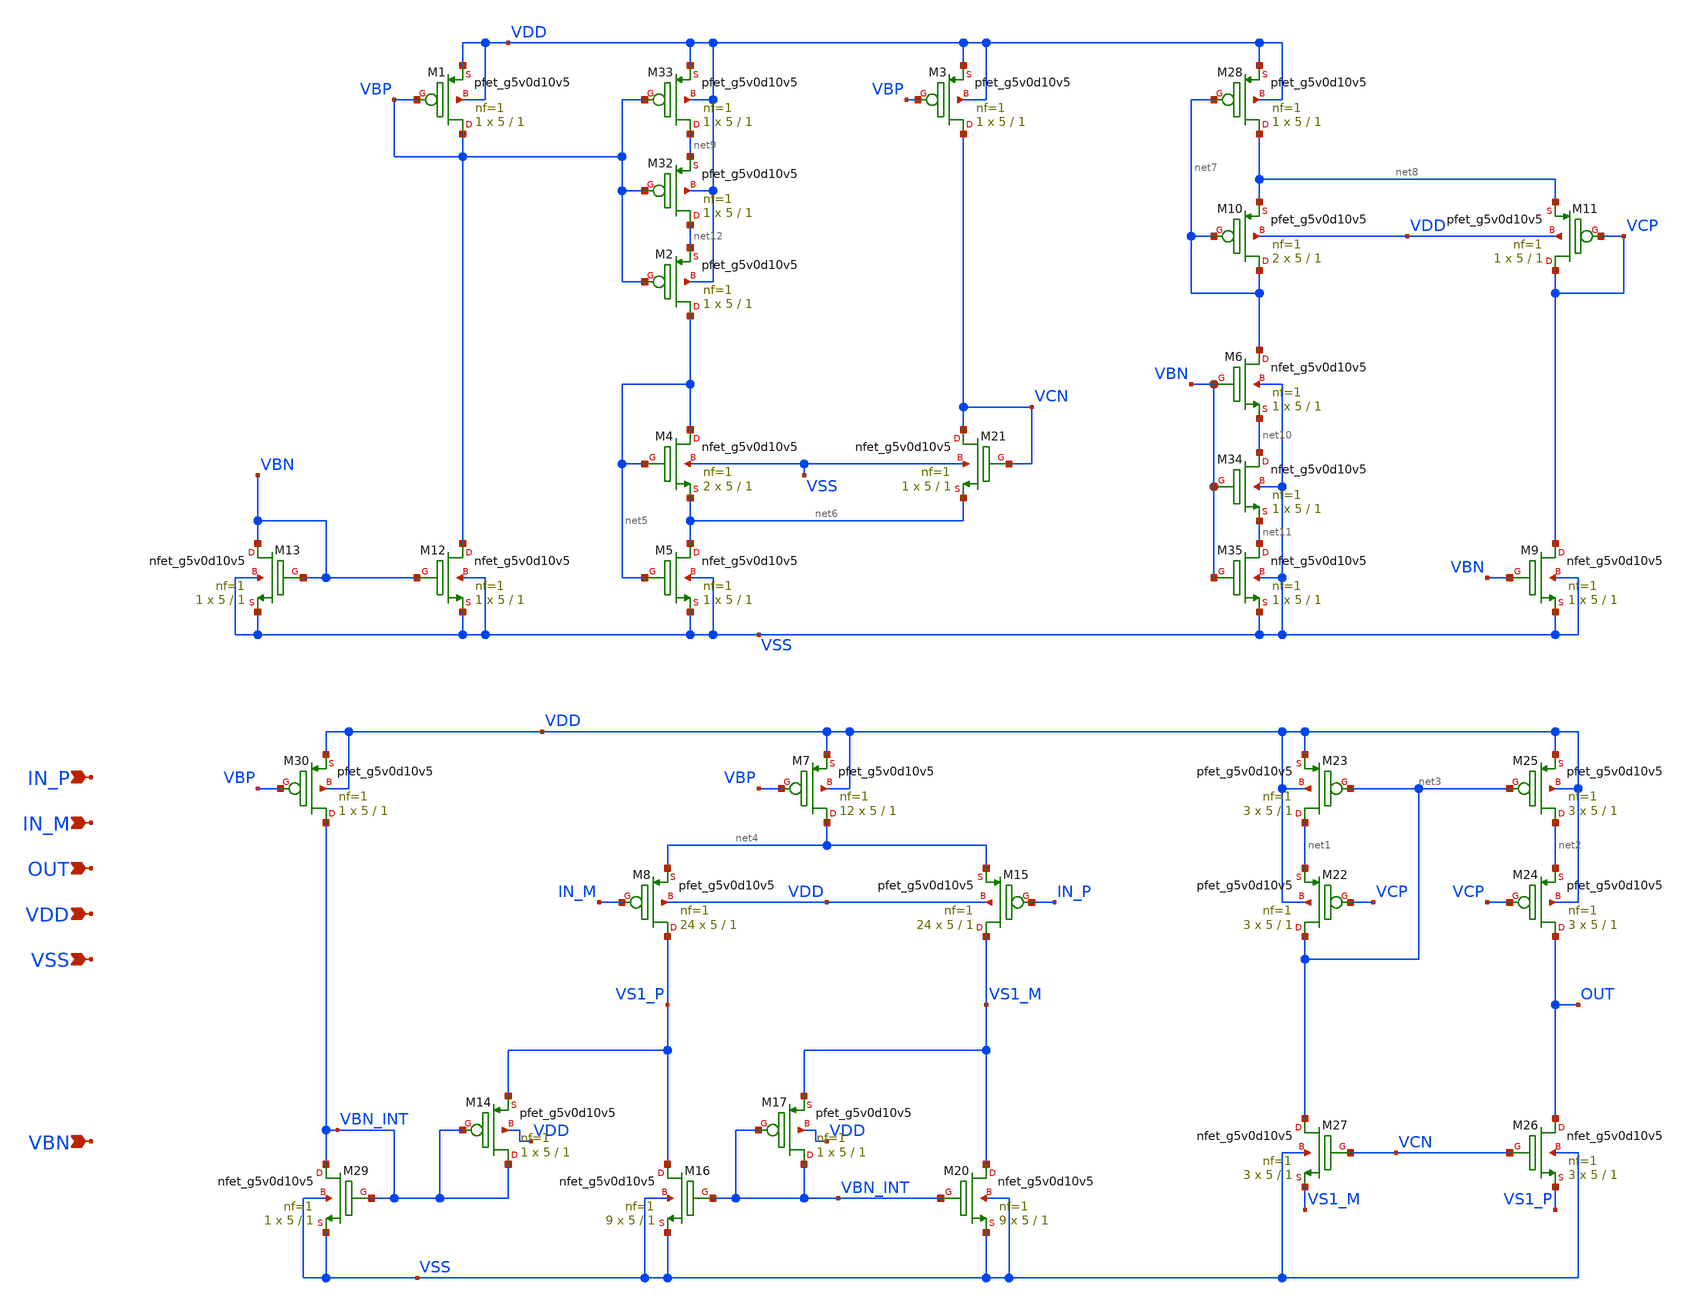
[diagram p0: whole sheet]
** sch_path: design/folded-cascode-p-in/folded_cascode_p_in.sch
**.subckt folded_cascode_p_in IN_P IN_M OUT VDD VSS VBN
*.ipin IN_P
*.ipin IN_M
*.ipin OUT
*.ipin VDD
*.ipin VSS
*.ipin VBN
XM7 net4 VBP VDD VDD sky130_fd_pr__pfet_g5v0d10v5 L=1 W=5 nf=1 ad='int((nf+1)/2) * W/nf * 0.29' as='int((nf+2)/2) * W/nf * 0.29'
+ pd='2*int((nf+1)/2) * (W/nf + 0.29)' ps='2*int((nf+2)/2) * (W/nf + 0.29)' nrd='0.29 / W' nrs='0.29 / W'
+ sa=0 sb=0 sd=0 mult=12 m=12
XM8 VS1_P IN_M net4 VDD sky130_fd_pr__pfet_g5v0d10v5 L=1 W=5 nf=1 ad='int((nf+1)/2) * W/nf * 0.29' as='int((nf+2)/2) * W/nf * 0.29'
+ pd='2*int((nf+1)/2) * (W/nf + 0.29)' ps='2*int((nf+2)/2) * (W/nf + 0.29)' nrd='0.29 / W' nrs='0.29 / W'
+ sa=0 sb=0 sd=0 mult=24 m=24
XM15 VS1_M IN_P net4 VDD sky130_fd_pr__pfet_g5v0d10v5 L=1 W=5 nf=1 ad='int((nf+1)/2) * W/nf * 0.29' as='int((nf+2)/2) * W/nf * 0.29'
+ pd='2*int((nf+1)/2) * (W/nf + 0.29)' ps='2*int((nf+2)/2) * (W/nf + 0.29)' nrd='0.29 / W' nrs='0.29 / W'
+ sa=0 sb=0 sd=0 mult=24 m=24
XM16 VS1_P VBN_INT VSS VSS sky130_fd_pr__nfet_g5v0d10v5 L=1 W=5 nf=1 ad='int((nf+1)/2) * W/nf * 0.29'
+ as='int((nf+2)/2) * W/nf * 0.29' pd='2*int((nf+1)/2) * (W/nf + 0.29)' ps='2*int((nf+2)/2) * (W/nf + 0.29)'
+ nrd='0.29 / W' nrs='0.29 / W' sa=0 sb=0 sd=0 mult=9 m=9
XM20 VS1_M VBN_INT VSS VSS sky130_fd_pr__nfet_g5v0d10v5 L=1 W=5 nf=1 ad='int((nf+1)/2) * W/nf * 0.29'
+ as='int((nf+2)/2) * W/nf * 0.29' pd='2*int((nf+1)/2) * (W/nf + 0.29)' ps='2*int((nf+2)/2) * (W/nf + 0.29)'
+ nrd='0.29 / W' nrs='0.29 / W' sa=0 sb=0 sd=0 mult=9 m=9
XM22 net3 VCP net1 VDD sky130_fd_pr__pfet_g5v0d10v5 L=1 W=5 nf=1 ad='int((nf+1)/2) * W/nf * 0.29' as='int((nf+2)/2) * W/nf * 0.29'
+ pd='2*int((nf+1)/2) * (W/nf + 0.29)' ps='2*int((nf+2)/2) * (W/nf + 0.29)' nrd='0.29 / W' nrs='0.29 / W'
+ sa=0 sb=0 sd=0 mult=3 m=3
XM23 net1 net3 VDD VDD sky130_fd_pr__pfet_g5v0d10v5 L=1 W=5 nf=1 ad='int((nf+1)/2) * W/nf * 0.29' as='int((nf+2)/2) * W/nf * 0.29'
+ pd='2*int((nf+1)/2) * (W/nf + 0.29)' ps='2*int((nf+2)/2) * (W/nf + 0.29)' nrd='0.29 / W' nrs='0.29 / W'
+ sa=0 sb=0 sd=0 mult=3 m=3
XM24 OUT VCP net2 VDD sky130_fd_pr__pfet_g5v0d10v5 L=1 W=5 nf=1 ad='int((nf+1)/2) * W/nf * 0.29' as='int((nf+2)/2) * W/nf * 0.29'
+ pd='2*int((nf+1)/2) * (W/nf + 0.29)' ps='2*int((nf+2)/2) * (W/nf + 0.29)' nrd='0.29 / W' nrs='0.29 / W'
+ sa=0 sb=0 sd=0 mult=3 m=3
XM25 net2 net3 VDD VDD sky130_fd_pr__pfet_g5v0d10v5 L=1 W=5 nf=1 ad='int((nf+1)/2) * W/nf * 0.29' as='int((nf+2)/2) * W/nf * 0.29'
+ pd='2*int((nf+1)/2) * (W/nf + 0.29)' ps='2*int((nf+2)/2) * (W/nf + 0.29)' nrd='0.29 / W' nrs='0.29 / W'
+ sa=0 sb=0 sd=0 mult=3 m=3
XM26 OUT VCN VS1_P VSS sky130_fd_pr__nfet_g5v0d10v5 L=1 W=5 nf=1 ad='int((nf+1)/2) * W/nf * 0.29' as='int((nf+2)/2) * W/nf * 0.29'
+ pd='2*int((nf+1)/2) * (W/nf + 0.29)' ps='2*int((nf+2)/2) * (W/nf + 0.29)' nrd='0.29 / W' nrs='0.29 / W'
+ sa=0 sb=0 sd=0 mult=3 m=3
XM27 net3 VCN VS1_M VSS sky130_fd_pr__nfet_g5v0d10v5 L=1 W=5 nf=1 ad='int((nf+1)/2) * W/nf * 0.29' as='int((nf+2)/2) * W/nf * 0.29'
+ pd='2*int((nf+1)/2) * (W/nf + 0.29)' ps='2*int((nf+2)/2) * (W/nf + 0.29)' nrd='0.29 / W' nrs='0.29 / W'
+ sa=0 sb=0 sd=0 mult=3 m=3
XM29 VBN_INT VBN_INT VSS VSS sky130_fd_pr__nfet_g5v0d10v5 L=1 W=5 nf=1 ad='int((nf+1)/2) * W/nf * 0.29'
+ as='int((nf+2)/2) * W/nf * 0.29' pd='2*int((nf+1)/2) * (W/nf + 0.29)' ps='2*int((nf+2)/2) * (W/nf + 0.29)'
+ nrd='0.29 / W' nrs='0.29 / W' sa=0 sb=0 sd=0 mult=1 m=1
XM30 VBN_INT VBP VDD VDD sky130_fd_pr__pfet_g5v0d10v5 L=1 W=5 nf=1 ad='int((nf+1)/2) * W/nf * 0.29' as='int((nf+2)/2) * W/nf * 0.29'
+ pd='2*int((nf+1)/2) * (W/nf + 0.29)' ps='2*int((nf+2)/2) * (W/nf + 0.29)' nrd='0.29 / W' nrs='0.29 / W'
+ sa=0 sb=0 sd=0 mult=1 m=1
XM1 VBP VBP VDD VDD sky130_fd_pr__pfet_g5v0d10v5 L=1 W=5 nf=1 ad='int((nf+1)/2) * W/nf * 0.29' as='int((nf+2)/2) * W/nf * 0.29'
+ pd='2*int((nf+1)/2) * (W/nf + 0.29)' ps='2*int((nf+2)/2) * (W/nf + 0.29)' nrd='0.29 / W' nrs='0.29 / W'
+ sa=0 sb=0 sd=0 mult=1 m=1
XM2 net5 VBP net12 VDD sky130_fd_pr__pfet_g5v0d10v5 L=1 W=5 nf=1 ad='int((nf+1)/2) * W/nf * 0.29' as='int((nf+2)/2) * W/nf * 0.29'
+ pd='2*int((nf+1)/2) * (W/nf + 0.29)' ps='2*int((nf+2)/2) * (W/nf + 0.29)' nrd='0.29 / W' nrs='0.29 / W'
+ sa=0 sb=0 sd=0 mult=1 m=1
XM3 VCN VBP VDD VDD sky130_fd_pr__pfet_g5v0d10v5 L=1 W=5 nf=1 ad='int((nf+1)/2) * W/nf * 0.29' as='int((nf+2)/2) * W/nf * 0.29'
+ pd='2*int((nf+1)/2) * (W/nf + 0.29)' ps='2*int((nf+2)/2) * (W/nf + 0.29)' nrd='0.29 / W' nrs='0.29 / W'
+ sa=0 sb=0 sd=0 mult=1 m=1
XM4 net5 net5 net6 VSS sky130_fd_pr__nfet_g5v0d10v5 L=1 W=5 nf=1 ad='int((nf+1)/2) * W/nf * 0.29' as='int((nf+2)/2) * W/nf * 0.29'
+ pd='2*int((nf+1)/2) * (W/nf + 0.29)' ps='2*int((nf+2)/2) * (W/nf + 0.29)' nrd='0.29 / W' nrs='0.29 / W'
+ sa=0 sb=0 sd=0 mult=2 m=2
XM5 net6 net5 VSS VSS sky130_fd_pr__nfet_g5v0d10v5 L=1 W=5 nf=1 ad='int((nf+1)/2) * W/nf * 0.29' as='int((nf+2)/2) * W/nf * 0.29'
+ pd='2*int((nf+1)/2) * (W/nf + 0.29)' ps='2*int((nf+2)/2) * (W/nf + 0.29)' nrd='0.29 / W' nrs='0.29 / W'
+ sa=0 sb=0 sd=0 mult=1 m=1
XM21 VCN VCN net6 VSS sky130_fd_pr__nfet_g5v0d10v5 L=1 W=5 nf=1 ad='int((nf+1)/2) * W/nf * 0.29' as='int((nf+2)/2) * W/nf * 0.29'
+ pd='2*int((nf+1)/2) * (W/nf + 0.29)' ps='2*int((nf+2)/2) * (W/nf + 0.29)' nrd='0.29 / W' nrs='0.29 / W'
+ sa=0 sb=0 sd=0 mult=1 m=1
XM6 net7 VBN net10 VSS sky130_fd_pr__nfet_g5v0d10v5 L=1 W=5 nf=1 ad='int((nf+1)/2) * W/nf * 0.29' as='int((nf+2)/2) * W/nf * 0.29'
+ pd='2*int((nf+1)/2) * (W/nf + 0.29)' ps='2*int((nf+2)/2) * (W/nf + 0.29)' nrd='0.29 / W' nrs='0.29 / W'
+ sa=0 sb=0 sd=0 mult=1 m=1
XM9 VCP VBN VSS VSS sky130_fd_pr__nfet_g5v0d10v5 L=1 W=5 nf=1 ad='int((nf+1)/2) * W/nf * 0.29' as='int((nf+2)/2) * W/nf * 0.29'
+ pd='2*int((nf+1)/2) * (W/nf + 0.29)' ps='2*int((nf+2)/2) * (W/nf + 0.29)' nrd='0.29 / W' nrs='0.29 / W'
+ sa=0 sb=0 sd=0 mult=1 m=1
XM10 net7 net7 net8 VDD sky130_fd_pr__pfet_g5v0d10v5 L=1 W=5 nf=1 ad='int((nf+1)/2) * W/nf * 0.29' as='int((nf+2)/2) * W/nf * 0.29'
+ pd='2*int((nf+1)/2) * (W/nf + 0.29)' ps='2*int((nf+2)/2) * (W/nf + 0.29)' nrd='0.29 / W' nrs='0.29 / W'
+ sa=0 sb=0 sd=0 mult=2 m=2
XM11 VCP VCP net8 VDD sky130_fd_pr__pfet_g5v0d10v5 L=1 W=5 nf=1 ad='int((nf+1)/2) * W/nf * 0.29' as='int((nf+2)/2) * W/nf * 0.29'
+ pd='2*int((nf+1)/2) * (W/nf + 0.29)' ps='2*int((nf+2)/2) * (W/nf + 0.29)' nrd='0.29 / W' nrs='0.29 / W'
+ sa=0 sb=0 sd=0 mult=1 m=1
XM28 net8 net7 VDD VDD sky130_fd_pr__pfet_g5v0d10v5 L=1 W=5 nf=1 ad='int((nf+1)/2) * W/nf * 0.29' as='int((nf+2)/2) * W/nf * 0.29'
+ pd='2*int((nf+1)/2) * (W/nf + 0.29)' ps='2*int((nf+2)/2) * (W/nf + 0.29)' nrd='0.29 / W' nrs='0.29 / W'
+ sa=0 sb=0 sd=0 mult=1 m=1
XM12 VBP VBN VSS VSS sky130_fd_pr__nfet_g5v0d10v5 L=1 W=5 nf=1 ad='int((nf+1)/2) * W/nf * 0.29' as='int((nf+2)/2) * W/nf * 0.29'
+ pd='2*int((nf+1)/2) * (W/nf + 0.29)' ps='2*int((nf+2)/2) * (W/nf + 0.29)' nrd='0.29 / W' nrs='0.29 / W'
+ sa=0 sb=0 sd=0 mult=1 m=1
XM32 net12 VBP net9 VDD sky130_fd_pr__pfet_g5v0d10v5 L=1 W=5 nf=1 ad='int((nf+1)/2) * W/nf * 0.29' as='int((nf+2)/2) * W/nf * 0.29'
+ pd='2*int((nf+1)/2) * (W/nf + 0.29)' ps='2*int((nf+2)/2) * (W/nf + 0.29)' nrd='0.29 / W' nrs='0.29 / W'
+ sa=0 sb=0 sd=0 mult=1 m=1
XM33 net9 VBP VDD VDD sky130_fd_pr__pfet_g5v0d10v5 L=1 W=5 nf=1 ad='int((nf+1)/2) * W/nf * 0.29' as='int((nf+2)/2) * W/nf * 0.29'
+ pd='2*int((nf+1)/2) * (W/nf + 0.29)' ps='2*int((nf+2)/2) * (W/nf + 0.29)' nrd='0.29 / W' nrs='0.29 / W'
+ sa=0 sb=0 sd=0 mult=1 m=1
XM34 net10 VBN net11 VSS sky130_fd_pr__nfet_g5v0d10v5 L=1 W=5 nf=1 ad='int((nf+1)/2) * W/nf * 0.29' as='int((nf+2)/2) * W/nf * 0.29'
+ pd='2*int((nf+1)/2) * (W/nf + 0.29)' ps='2*int((nf+2)/2) * (W/nf + 0.29)' nrd='0.29 / W' nrs='0.29 / W'
+ sa=0 sb=0 sd=0 mult=1 m=1
XM35 net11 VBN VSS VSS sky130_fd_pr__nfet_g5v0d10v5 L=1 W=5 nf=1 ad='int((nf+1)/2) * W/nf * 0.29' as='int((nf+2)/2) * W/nf * 0.29'
+ pd='2*int((nf+1)/2) * (W/nf + 0.29)' ps='2*int((nf+2)/2) * (W/nf + 0.29)' nrd='0.29 / W' nrs='0.29 / W'
+ sa=0 sb=0 sd=0 mult=1 m=1
XM13 VBN VBN VSS VSS sky130_fd_pr__nfet_g5v0d10v5 L=1 W=5 nf=1 ad='int((nf+1)/2) * W/nf * 0.29' as='int((nf+2)/2) * W/nf * 0.29'
+ pd='2*int((nf+1)/2) * (W/nf + 0.29)' ps='2*int((nf+2)/2) * (W/nf + 0.29)' nrd='0.29 / W' nrs='0.29 / W'
+ sa=0 sb=0 sd=0 mult=1 m=1
XM14 VBN_INT VBN_INT VS1_P VDD sky130_fd_pr__pfet_g5v0d10v5 L=1 W=5 nf=1 ad='int((nf+1)/2) * W/nf * 0.29'
+ as='int((nf+2)/2) * W/nf * 0.29' pd='2*int((nf+1)/2) * (W/nf + 0.29)' ps='2*int((nf+2)/2) * (W/nf + 0.29)'
+ nrd='0.29 / W' nrs='0.29 / W' sa=0 sb=0 sd=0 mult=1 m=1
XM17 VBN_INT VBN_INT VS1_M VDD sky130_fd_pr__pfet_g5v0d10v5 L=1 W=5 nf=1 ad='int((nf+1)/2) * W/nf * 0.29'
+ as='int((nf+2)/2) * W/nf * 0.29' pd='2*int((nf+1)/2) * (W/nf + 0.29)' ps='2*int((nf+2)/2) * (W/nf + 0.29)'
+ nrd='0.29 / W' nrs='0.29 / W' sa=0 sb=0 sd=0 mult=1 m=1
**.ends
.end
